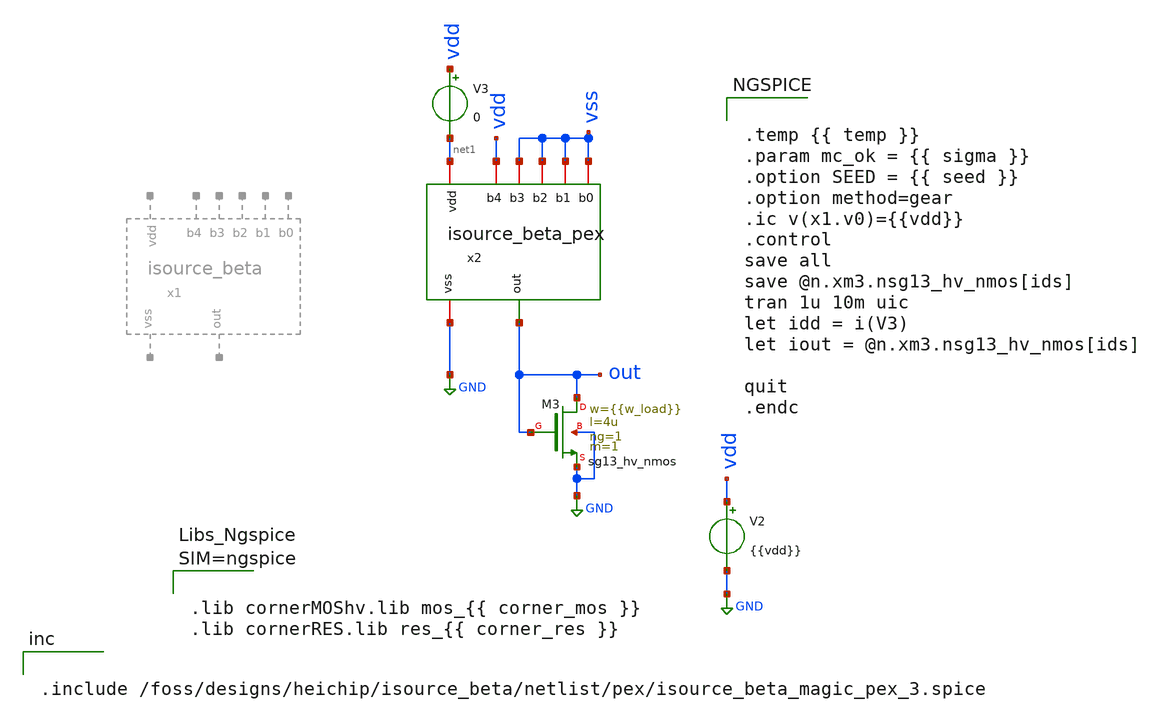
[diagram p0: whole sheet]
** sch_path: testbenches/xschem/tb_isource_beta_tran.sch
**.subckt tb_isource_beta_tran
V2 vdd GND {{vdd}}
V3 vdd net1 0
.save i(v3)
XM3 out out GND GND sg13_hv_nmos w={{w_load}} l=4u ng=1 m=1 mm_ok=1
x2 vss net1 vss out vss vss GND vdd isource_beta_pex
**** begin user architecture code


.temp {{ temp }}
.param mc_ok = {{ sigma }}
.option SEED = {{ seed }}
.option method=gear
.ic v(x1.v0)={{vdd}}
.control
save all
save @n.xm3.nsg13_hv_nmos[ids]
tran 1u 10m uic
let idd = i(V3)
let iout = @n.xm3.nsg13_hv_nmos[ids]

quit
.endc





.lib cornerMOShv.lib mos_{{ corner_mos }}
.lib cornerRES.lib res_{{ corner_res }}





.include /foss/designs/heichip/isource_beta/netlist/pex/isource_beta_magic_pex_3.spice


**** end user architecture code
**.ends

* expanding   symbol:  heichip/isource_beta/schematic/xschem/isource_beta.sym # of pins=8
** sym_path: schematic/xschem/isource_beta.sym
** sch_path: schematic/xschem/isource_beta.sch
.subckt isource_beta b0 vdd b1 out b2 b3 vss b4
*.opin out
*.iopin vdd
*.iopin vss
*.iopin b0
*.iopin b1
*.iopin b2
*.iopin b3
*.iopin b4
XM1 net1 v0 vdd vdd sg13_hv_pmos w=12u l=4u ng=4 m=1 mm_ok=1
XM2 v0 v0 vdd vdd sg13_hv_pmos w=12u l=4u ng=4 m=1 mm_ok=1
XM3 net1 net1 vss vss sg13_hv_nmos w=40u l=4u ng=10 m=1 mm_ok=1
XM4 v0 net1 iref vss sg13_hv_nmos w=40u l=4u ng=10 m=3 mm_ok=1
XM5 out v0 vdd vdd sg13_hv_pmos w=12u l=4u ng=4 m=1 mm_ok=1
XMS1 net2 vdd vdd vdd sg13_hv_pmos w=0.5u l=10u ng=1 m=1 mm_ok=1
XMS2 net2 net1 vss vss sg13_hv_nmos w=10u l=0.45u ng=1 m=1 mm_ok=1
XMS3 v0 net2 vss vss sg13_hv_nmos w=10u l=0.45u ng=1 m=1 mm_ok=1
XR10 iref net4 vss rppd w=1e-6 l=160e-6 m=1 b=0 mm_ok=1
XR2 net6 vss vss rppd w=1e-6 l=10e-6 m=1 b=0 mm_ok=1
XM6 iref b4 net4 vss sg13_hv_nmos w=16u l=0.45u ng=2 m=1 mm_ok=1
XR3 net5 net6 vss rppd w=1e-6 l=20e-6 m=1 b=0 mm_ok=1
XR4 net3 net5 vss rppd w=1e-6 l=40e-6 m=1 b=0 mm_ok=1
XR5 net4 net3 vss rppd w=1e-6 l=80e-6 m=1 b=0 mm_ok=1
XM7 net4 b3 net3 vss sg13_hv_nmos w=16u l=0.45u ng=2 m=1 mm_ok=1
XM8 net3 b2 net5 vss sg13_hv_nmos w=16u l=0.45u ng=2 m=1 mm_ok=1
XM9 net5 b1 net6 vss sg13_hv_nmos w=16u l=0.45u ng=2 m=1 mm_ok=1
XM10 net6 b0 vss vss sg13_hv_nmos w=16u l=0.45u ng=2 m=1 mm_ok=1
.ends

.GLOBAL GND
.end
